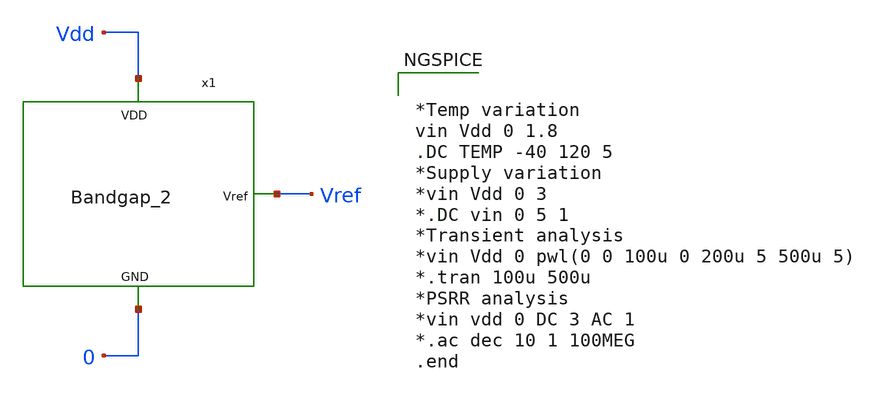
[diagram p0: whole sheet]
** sch_path: Analog_Blocks/Bandgap/Testbench/Bandgap_2_TB.sch
**.subckt Bandgap_2_TB
x1 Vdd Vref 0 Bandgap_2
**** begin user architecture code


*Temp variation
vin Vdd 0 1.8
.DC TEMP -40 120 5
*Supply variation
*vin Vdd 0 3
*.DC vin 0 5 1
*Transient analysis
*vin Vdd 0 pwl(0 0 100u 0 200u 5 500u 5)
*.tran 100u 500u
*PSRR analysis
*vin vdd 0 DC 3 AC 1
*.ac dec 10 1 100MEG
.end



.include $::SKYWATER_MODELS/cells/nfet_01v8/sky130_fd_pr__nfet_01v8__tt.corner.spice
.include $::SKYWATER_MODELS/cells/nfet_01v8_lvt/sky130_fd_pr__nfet_01v8_lvt__tt.corner.spice
.include $::SKYWATER_MODELS/cells/pfet_01v8/sky130_fd_pr__pfet_01v8__tt.corner.spice
.include $::SKYWATER_MODELS/cells/nfet_03v3_nvt/sky130_fd_pr__nfet_03v3_nvt__tt.corner.spice
.include $::SKYWATER_MODELS/cells/nfet_05v0_nvt/sky130_fd_pr__nfet_05v0_nvt__tt.corner.spice
.include $::SKYWATER_MODELS/cells/esd_nfet_01v8/sky130_fd_pr__esd_nfet_01v8__tt.corner.spice
.include $::SKYWATER_MODELS/cells/pfet_01v8_lvt/sky130_fd_pr__pfet_01v8_lvt__tt.corner.spice
.include $::SKYWATER_MODELS/cells/pfet_01v8_hvt/sky130_fd_pr__pfet_01v8_hvt__tt.corner.spice
.include $::SKYWATER_MODELS/cells/esd_pfet_g5v0d10v5/sky130_fd_pr__esd_pfet_g5v0d10v5__tt.corner.spice
.include $::SKYWATER_MODELS/cells/pfet_g5v0d10v5/sky130_fd_pr__pfet_g5v0d10v5__tt.corner.spice
.include $::SKYWATER_MODELS/cells/pfet_g5v0d16v0/sky130_fd_pr__pfet_g5v0d16v0__tt.corner.spice
.include $::SKYWATER_MODELS/cells/nfet_g5v0d10v5/sky130_fd_pr__nfet_g5v0d10v5__tt.corner.spice
.include $::SKYWATER_MODELS/cells/nfet_g5v0d16v0/sky130_fd_pr__nfet_g5v0d16v0__tt_discrete.corner.spice
.include $::SKYWATER_MODELS/cells/esd_nfet_g5v0d10v5/sky130_fd_pr__esd_nfet_g5v0d10v5__tt.corner.spice
.include $::SKYWATER_MODELS/models/corners/tt/nonfet.spice
* Mismatch parameters
.include $::SKYWATER_MODELS/cells/nfet_01v8/sky130_fd_pr__nfet_01v8__mismatch.corner.spice
.include $::SKYWATER_MODELS/cells/pfet_01v8/sky130_fd_pr__pfet_01v8__mismatch.corner.spice
.include $::SKYWATER_MODELS/cells/nfet_01v8_lvt/sky130_fd_pr__nfet_01v8_lvt__mismatch.corner.spice
.include $::SKYWATER_MODELS/cells/pfet_01v8_lvt/sky130_fd_pr__pfet_01v8_lvt__mismatch.corner.spice
.include $::SKYWATER_MODELS/cells/pfet_01v8_hvt/sky130_fd_pr__pfet_01v8_hvt__mismatch.corner.spice
.include $::SKYWATER_MODELS/cells/nfet_g5v0d10v5/sky130_fd_pr__nfet_g5v0d10v5__mismatch.corner.spice
.include $::SKYWATER_MODELS/cells/pfet_g5v0d10v5/sky130_fd_pr__pfet_g5v0d10v5__mismatch.corner.spice
.include $::SKYWATER_MODELS/cells/nfet_05v0_nvt/sky130_fd_pr__nfet_05v0_nvt__mismatch.corner.spice
.include $::SKYWATER_MODELS/cells/nfet_03v3_nvt/sky130_fd_pr__nfet_03v3_nvt__mismatch.corner.spice
* Resistor$::SKYWATER_MODELS/Capacitor
.include $::SKYWATER_MODELS/models/r+c/res_typical__cap_typical.spice
.include $::SKYWATER_MODELS/models/r+c/res_typical__cap_typical__lin.spice
* Special cells
.include $::SKYWATER_MODELS/models/corners/tt/specialized_cells.spice
* All models
.include $::SKYWATER_MODELS/models/all.spice
* Corner
.include $::SKYWATER_MODELS/models/corners/tt/rf.spice

**** end user architecture code
**.ends

* expanding   symbol:
*+  /home/eslam/Analog_Design/Analog_Blocks/Bandgap/Schematics/BGR_2/Bandgap_2.sym # of pins=3
** sym_path: Analog_Blocks/Bandgap/Schematics/BGR1.8v_2/Bandgap_2.sym
** sch_path: Analog_Blocks/Bandgap/Schematics/BGR1.8v_2/Bandgap_2.sch
.subckt Bandgap_2 VDD Vref GND
*.ipin VDD
*.ipin GND
*.opin Vref
XM13 Vref net1 VDD VDD sky130_fd_pr__pfet_g5v0d10v5 L=0.5 W=5 nf=1 ad='int((nf+1)/2) * W/nf * 0.29' as='int((nf+2)/2) * W/nf * 0.29'
+ pd='2*int((nf+1)/2) * (W/nf + 0.29)' ps='2*int((nf+2)/2) * (W/nf + 0.29)' nrd='0.29 / W' nrs='0.29 / W'
+ sa=0 sb=0 sd=0 mult=4 m=4
XM14 net9 net1 VDD VDD sky130_fd_pr__pfet_g5v0d10v5 L=0.5 W=5 nf=1 ad='int((nf+1)/2) * W/nf * 0.29' as='int((nf+2)/2) * W/nf * 0.29'
+ pd='2*int((nf+1)/2) * (W/nf + 0.29)' ps='2*int((nf+2)/2) * (W/nf + 0.29)' nrd='0.29 / W' nrs='0.29 / W'
+ sa=0 sb=0 sd=0 mult=4 m=4
XQ10 GND GND net4 sky130_fd_pr__pnp_05v5_W0p68L0p68 m=1
XQ11 GND GND net2 sky130_fd_pr__pnp_05v5_W0p68L0p68 m=1
XQ12 GND GND net2 sky130_fd_pr__pnp_05v5_W0p68L0p68 m=1
XQ13 GND GND net2 sky130_fd_pr__pnp_05v5_W0p68L0p68 m=1
XQ14 GND GND net2 sky130_fd_pr__pnp_05v5_W0p68L0p68 m=1
XQ15 GND GND net2 sky130_fd_pr__pnp_05v5_W0p68L0p68 m=1
XQ16 GND GND net2 sky130_fd_pr__pnp_05v5_W0p68L0p68 m=1
XQ17 GND GND net2 sky130_fd_pr__pnp_05v5_W0p68L0p68 m=1
XQ18 GND GND net2 sky130_fd_pr__pnp_05v5_W0p68L0p68 m=1
XR4 net2 net3 GND sky130_fd_pr__res_xhigh_po_1p41 L=1.8 mult=1 m=1
XM15 net6 net1 VDD VDD sky130_fd_pr__pfet_g5v0d10v5 L=0.5 W=1 nf=1 ad='int((nf+1)/2) * W/nf * 0.29' as='int((nf+2)/2) * W/nf * 0.29'
+ pd='2*int((nf+1)/2) * (W/nf + 0.29)' ps='2*int((nf+2)/2) * (W/nf + 0.29)' nrd='0.29 / W' nrs='0.29 / W'
+ sa=0 sb=0 sd=0 mult=4 m=4
XM16 net1 net1 VDD VDD sky130_fd_pr__pfet_g5v0d10v5 L=0.5 W=1 nf=1 ad='int((nf+1)/2) * W/nf * 0.29' as='int((nf+2)/2) * W/nf * 0.29'
+ pd='2*int((nf+1)/2) * (W/nf + 0.29)' ps='2*int((nf+2)/2) * (W/nf + 0.29)' nrd='0.29 / W' nrs='0.29 / W'
+ sa=0 sb=0 sd=0 mult=44 m=44
XM17 net7 net3 net6 VDD sky130_fd_pr__pfet_g5v0d10v5 L=0.5 W=15 nf=1 ad='int((nf+1)/2) * W/nf * 0.29'
+ as='int((nf+2)/2) * W/nf * 0.29' pd='2*int((nf+1)/2) * (W/nf + 0.29)' ps='2*int((nf+2)/2) * (W/nf + 0.29)'
+ nrd='0.29 / W' nrs='0.29 / W' sa=0 sb=0 sd=0 mult=6 m=6
XM18 net5 net4 net6 VDD sky130_fd_pr__pfet_g5v0d10v5 L=0.5 W=15 nf=1 ad='int((nf+1)/2) * W/nf * 0.29'
+ as='int((nf+2)/2) * W/nf * 0.29' pd='2*int((nf+1)/2) * (W/nf + 0.29)' ps='2*int((nf+2)/2) * (W/nf + 0.29)'
+ nrd='0.29 / W' nrs='0.29 / W' sa=0 sb=0 sd=0 mult=6 m=6
XM19 net1 net7 GND GND sky130_fd_pr__nfet_g5v0d10v5 L=0.5 W=0.42 nf=1 ad='int((nf+1)/2) * W/nf * 0.29'
+ as='int((nf+2)/2) * W/nf * 0.29' pd='2*int((nf+1)/2) * (W/nf + 0.29)' ps='2*int((nf+2)/2) * (W/nf + 0.29)'
+ nrd='0.29 / W' nrs='0.29 / W' sa=0 sb=0 sd=0 mult=10 m=10
XM20 net7 net5 GND GND sky130_fd_pr__nfet_g5v0d10v5 L=0.5 W=0.42 nf=1 ad='int((nf+1)/2) * W/nf * 0.29'
+ as='int((nf+2)/2) * W/nf * 0.29' pd='2*int((nf+1)/2) * (W/nf + 0.29)' ps='2*int((nf+2)/2) * (W/nf + 0.29)'
+ nrd='0.29 / W' nrs='0.29 / W' sa=0 sb=0 sd=0 mult=4 m=4
XM21 net5 net5 GND GND sky130_fd_pr__nfet_g5v0d10v5 L=0.5 W=0.42 nf=1 ad='int((nf+1)/2) * W/nf * 0.29'
+ as='int((nf+2)/2) * W/nf * 0.29' pd='2*int((nf+1)/2) * (W/nf + 0.29)' ps='2*int((nf+2)/2) * (W/nf + 0.29)'
+ nrd='0.29 / W' nrs='0.29 / W' sa=0 sb=0 sd=0 mult=4 m=4
XM22 net8 net1 VDD VDD sky130_fd_pr__pfet_g5v0d10v5 L=1 W=20 nf=1 ad='int((nf+1)/2) * W/nf * 0.29' as='int((nf+2)/2) * W/nf * 0.29'
+ pd='2*int((nf+1)/2) * (W/nf + 0.29)' ps='2*int((nf+2)/2) * (W/nf + 0.29)' nrd='0.29 / W' nrs='0.29 / W'
+ sa=0 sb=0 sd=0 mult=2 m=2
XM23 net8 net1 GND GND sky130_fd_pr__nfet_g5v0d10v5 L=20 W=0.42 nf=1 ad='int((nf+1)/2) * W/nf * 0.29'
+ as='int((nf+2)/2) * W/nf * 0.29' pd='2*int((nf+1)/2) * (W/nf + 0.29)' ps='2*int((nf+2)/2) * (W/nf + 0.29)'
+ nrd='0.29 / W' nrs='0.29 / W' sa=0 sb=0 sd=0 mult=1 m=1
XM24 net4 net8 VDD VDD sky130_fd_pr__pfet_g5v0d10v5 L=1 W=20 nf=1 ad='int((nf+1)/2) * W/nf * 0.29' as='int((nf+2)/2) * W/nf * 0.29'
+ pd='2*int((nf+1)/2) * (W/nf + 0.29)' ps='2*int((nf+2)/2) * (W/nf + 0.29)' nrd='0.29 / W' nrs='0.29 / W'
+ sa=0 sb=0 sd=0 mult=2 m=2
XR1 net3 Vref GND sky130_fd_pr__res_xhigh_po_1p41 L=7.2 mult=1 m=1
XR2 net4 net9 GND sky130_fd_pr__res_xhigh_po_1p41 L=7.2 mult=1 m=1
.ends

.end
